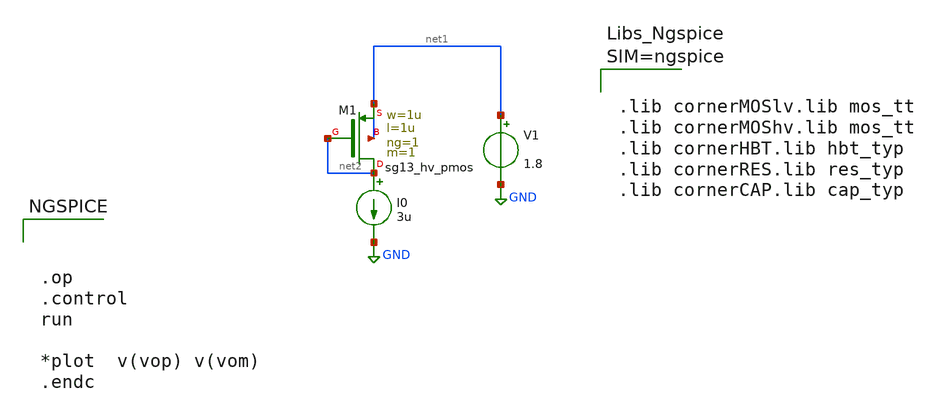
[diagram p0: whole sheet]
** sch_path: dependencies/OTA/OTA-main/schematic/xschem/temp2.sch
**.subckt temp2
V1 net1 GND 1.8
XM1 net2 net2 net1 net1 sg13_hv_pmos w=1u l=1u ng=1 m=1 mm_ok=1
I0 net2 GND 3u
**** begin user architecture code



.lib cornerMOSlv.lib mos_tt
.lib cornerMOShv.lib mos_tt
.lib cornerHBT.lib hbt_typ
.lib cornerRES.lib res_typ
.lib cornerCAP.lib cap_typ






.op
.control
run

*plot  v(vop) v(vom)
.endc


**** end user architecture code
**.ends
.GLOBAL GND
.end
